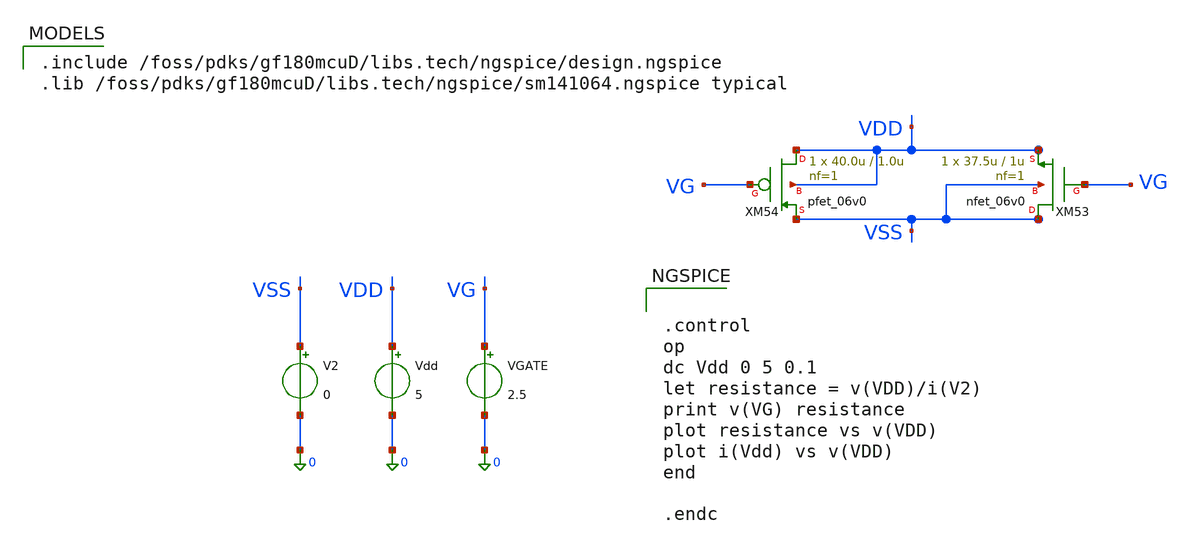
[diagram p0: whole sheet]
** sch_path: activities/opamp3An/RinLinearityCheck.sch
**.subckt RinLinearityCheck
XM53 VSS VG VDD VSS nfet_06v0 L=1u W=37.5u nf=1 ad='int((nf+1)/2) * W/nf * 0.18u' as='int((nf+2)/2) * W/nf * 0.18u'
+ pd='2*int((nf+1)/2) * (W/nf + 0.18u)' ps='2*int((nf+2)/2) * (W/nf + 0.18u)' nrd='0.18u / W' nrs='0.18u / W'
+ sa=0 sb=0 sd=0 m=1
XM54 VDD VG VSS VDD pfet_06v0 L=1.0u W=40.0u nf=1 ad='int((nf+1)/2) * W/nf * 0.18u' as='int((nf+2)/2) * W/nf * 0.18u'
+ pd='2*int((nf+1)/2) * (W/nf + 0.18u)' ps='2*int((nf+2)/2) * (W/nf + 0.18u)' nrd='0.18u / W' nrs='0.18u / W'
+ sa=0 sb=0 sd=0 m=1
V2 VSS 0 0
Vdd VDD 0 5
VGATE VG 0 2.5
**** begin user architecture code

.include /foss/pdks/gf180mcuD/libs.tech/ngspice/design.ngspice
.lib /foss/pdks/gf180mcuD/libs.tech/ngspice/sm141064.ngspice typical



.control
op
dc Vdd 0 5 0.1
let resistance = v(VDD)/i(V2)
print v(VG) resistance
plot resistance vs v(VDD)
plot i(Vdd) vs v(VDD)
end

.endc

**** end user architecture code
**.ends
.end
